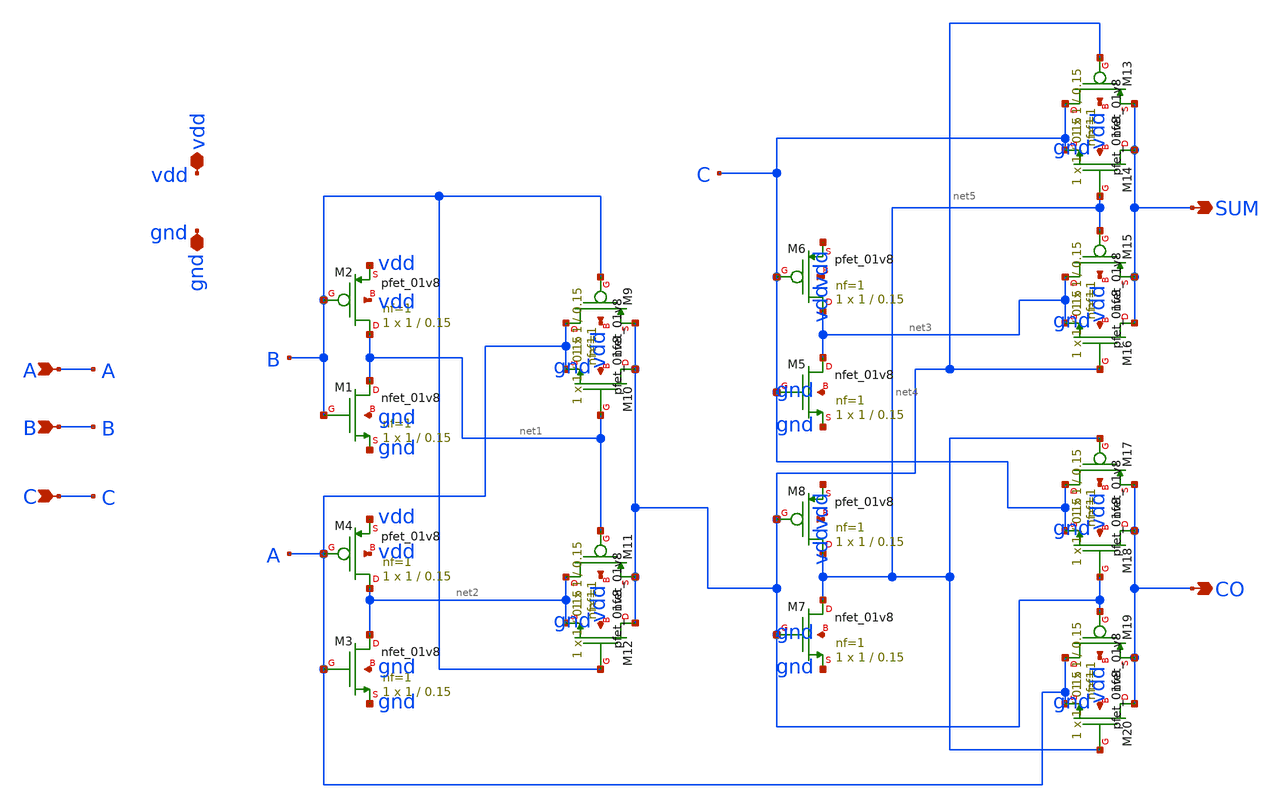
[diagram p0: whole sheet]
** sch_path: FA20T.sch
**.subckt FA20T A B C SUM CO vdd gnd
*.ipin A
*.ipin B
*.ipin C
*.opin SUM
*.opin CO
*.iopin vdd
*.iopin gnd
XM1 net1 B gnd gnd sky130_fd_pr__nfet_01v8 L=0.15 W=1 nf=1 ad='int((1 + 1)/2) * 1 / 1 * 0.29' as='int((1 + 2)/2) * 1 / 1 * 0.29'
+ pd='2*int((1 + 1)/2) * (1 / 1 + 0.29)' ps='2*int((1 + 2)/2) * (1 / 1 + 0.29)' nrd='0.29 / 1 ' nrs='0.29 / 1 '
+ sa=0 sb=0 sd=0 mult=1 m=1
XM2 net1 B vdd vdd sky130_fd_pr__pfet_01v8 L=0.15 W=1 nf=1 ad='int((1 + 1)/2) * 1 / 1 * 0.29' as='int((1 + 2)/2) * 1 / 1 * 0.29'
+ pd='2*int((1 + 1)/2) * (1 / 1 + 0.29)' ps='2*int((1 + 2)/2) * (1 / 1 + 0.29)' nrd='0.29 / 1 ' nrs='0.29 / 1 '
+ sa=0 sb=0 sd=0 mult=1 m=1
XM3 net2 A gnd gnd sky130_fd_pr__nfet_01v8 L=0.15 W=1 nf=1 ad='int((1 + 1)/2) * 1 / 1 * 0.29' as='int((1 + 2)/2) * 1 / 1 * 0.29'
+ pd='2*int((1 + 1)/2) * (1 / 1 + 0.29)' ps='2*int((1 + 2)/2) * (1 / 1 + 0.29)' nrd='0.29 / 1 ' nrs='0.29 / 1 '
+ sa=0 sb=0 sd=0 mult=1 m=1
XM4 net2 A vdd vdd sky130_fd_pr__pfet_01v8 L=0.15 W=1 nf=1 ad='int((1 + 1)/2) * 1 / 1 * 0.29' as='int((1 + 2)/2) * 1 / 1 * 0.29'
+ pd='2*int((1 + 1)/2) * (1 / 1 + 0.29)' ps='2*int((1 + 2)/2) * (1 / 1 + 0.29)' nrd='0.29 / 1 ' nrs='0.29 / 1 '
+ sa=0 sb=0 sd=0 mult=1 m=1
XM5 net3 C gnd gnd sky130_fd_pr__nfet_01v8 L=0.15 W=1 nf=1 ad='int((1 + 1)/2) * 1 / 1 * 0.29' as='int((1 + 2)/2) * 1 / 1 * 0.29'
+ pd='2*int((1 + 1)/2) * (1 / 1 + 0.29)' ps='2*int((1 + 2)/2) * (1 / 1 + 0.29)' nrd='0.29 / 1 ' nrs='0.29 / 1 '
+ sa=0 sb=0 sd=0 mult=1 m=1
XM6 net3 C vdd vdd sky130_fd_pr__pfet_01v8 L=0.15 W=1 nf=1 ad='int((1 + 1)/2) * 1 / 1 * 0.29' as='int((1 + 2)/2) * 1 / 1 * 0.29'
+ pd='2*int((1 + 1)/2) * (1 / 1 + 0.29)' ps='2*int((1 + 2)/2) * (1 / 1 + 0.29)' nrd='0.29 / 1 ' nrs='0.29 / 1 '
+ sa=0 sb=0 sd=0 mult=1 m=1
XM7 net4 net5 gnd gnd sky130_fd_pr__nfet_01v8 L=0.15 W=1 nf=1 ad='int((1 + 1)/2) * 1 / 1 * 0.29' as='int((1 + 2)/2) * 1 / 1 * 0.29'
+ pd='2*int((1 + 1)/2) * (1 / 1 + 0.29)' ps='2*int((1 + 2)/2) * (1 / 1 + 0.29)' nrd='0.29 / 1 ' nrs='0.29 / 1 '
+ sa=0 sb=0 sd=0 mult=1 m=1
XM8 net4 net5 vdd vdd sky130_fd_pr__pfet_01v8 L=0.15 W=1 nf=1 ad='int((1 + 1)/2) * 1 / 1 * 0.29' as='int((1 + 2)/2) * 1 / 1 * 0.29'
+ pd='2*int((1 + 1)/2) * (1 / 1 + 0.29)' ps='2*int((1 + 2)/2) * (1 / 1 + 0.29)' nrd='0.29 / 1 ' nrs='0.29 / 1 '
+ sa=0 sb=0 sd=0 mult=1 m=1
XM9 A B net5 vdd sky130_fd_pr__pfet_01v8 L=0.15 W=1 nf=1 ad='int((1 + 1)/2) * 1 / 1 * 0.29' as='int((1 + 2)/2) * 1 / 1 * 0.29'
+ pd='2*int((1 + 1)/2) * (1 / 1 + 0.29)' ps='2*int((1 + 2)/2) * (1 / 1 + 0.29)' nrd='0.29 / 1 ' nrs='0.29 / 1 '
+ sa=0 sb=0 sd=0 mult=1 m=1
XM10 net5 net1 A gnd sky130_fd_pr__nfet_01v8 L=0.15 W=1 nf=1 ad='int((1 + 1)/2) * 1 / 1 * 0.29' as='int((1 + 2)/2) * 1 / 1 * 0.29'
+ pd='2*int((1 + 1)/2) * (1 / 1 + 0.29)' ps='2*int((1 + 2)/2) * (1 / 1 + 0.29)' nrd='0.29 / 1 ' nrs='0.29 / 1 '
+ sa=0 sb=0 sd=0 mult=1 m=1
XM11 net2 net1 net5 vdd sky130_fd_pr__pfet_01v8 L=0.15 W=1 nf=1 ad='int((1 + 1)/2) * 1 / 1 * 0.29' as='int((1 + 2)/2) * 1 / 1 * 0.29'
+ pd='2*int((1 + 1)/2) * (1 / 1 + 0.29)' ps='2*int((1 + 2)/2) * (1 / 1 + 0.29)' nrd='0.29 / 1 ' nrs='0.29 / 1 '
+ sa=0 sb=0 sd=0 mult=1 m=1
XM12 net5 B net2 gnd sky130_fd_pr__nfet_01v8 L=0.15 W=1 nf=1 ad='int((1 + 1)/2) * 1 / 1 * 0.29' as='int((1 + 2)/2) * 1 / 1 * 0.29'
+ pd='2*int((1 + 1)/2) * (1 / 1 + 0.29)' ps='2*int((1 + 2)/2) * (1 / 1 + 0.29)' nrd='0.29 / 1 ' nrs='0.29 / 1 '
+ sa=0 sb=0 sd=0 mult=1 m=1
XM13 C net5 SUM vdd sky130_fd_pr__pfet_01v8 L=0.15 W=1 nf=1 ad='int((1 + 1)/2) * 1 / 1 * 0.29' as='int((1 + 2)/2) * 1 / 1 * 0.29'
+ pd='2*int((1 + 1)/2) * (1 / 1 + 0.29)' ps='2*int((1 + 2)/2) * (1 / 1 + 0.29)' nrd='0.29 / 1 ' nrs='0.29 / 1 '
+ sa=0 sb=0 sd=0 mult=1 m=1
XM14 SUM net4 C gnd sky130_fd_pr__nfet_01v8 L=0.15 W=1 nf=1 ad='int((1 + 1)/2) * 1 / 1 * 0.29' as='int((1 + 2)/2) * 1 / 1 * 0.29'
+ pd='2*int((1 + 1)/2) * (1 / 1 + 0.29)' ps='2*int((1 + 2)/2) * (1 / 1 + 0.29)' nrd='0.29 / 1 ' nrs='0.29 / 1 '
+ sa=0 sb=0 sd=0 mult=1 m=1
XM15 net3 net4 SUM vdd sky130_fd_pr__pfet_01v8 L=0.15 W=1 nf=1 ad='int((1 + 1)/2) * 1 / 1 * 0.29' as='int((1 + 2)/2) * 1 / 1 * 0.29'
+ pd='2*int((1 + 1)/2) * (1 / 1 + 0.29)' ps='2*int((1 + 2)/2) * (1 / 1 + 0.29)' nrd='0.29 / 1 ' nrs='0.29 / 1 '
+ sa=0 sb=0 sd=0 mult=1 m=1
XM16 SUM net5 net3 gnd sky130_fd_pr__nfet_01v8 L=0.15 W=1 nf=1 ad='int((1 + 1)/2) * 1 / 1 * 0.29' as='int((1 + 2)/2) * 1 / 1 * 0.29'
+ pd='2*int((1 + 1)/2) * (1 / 1 + 0.29)' ps='2*int((1 + 2)/2) * (1 / 1 + 0.29)' nrd='0.29 / 1 ' nrs='0.29 / 1 '
+ sa=0 sb=0 sd=0 mult=1 m=1
XM17 C net4 CO vdd sky130_fd_pr__pfet_01v8 L=0.15 W=1 nf=1 ad='int((1 + 1)/2) * 1 / 1 * 0.29' as='int((1 + 2)/2) * 1 / 1 * 0.29'
+ pd='2*int((1 + 1)/2) * (1 / 1 + 0.29)' ps='2*int((1 + 2)/2) * (1 / 1 + 0.29)' nrd='0.29 / 1 ' nrs='0.29 / 1 '
+ sa=0 sb=0 sd=0 mult=1 m=1
XM18 CO net5 C gnd sky130_fd_pr__nfet_01v8 L=0.15 W=1 nf=1 ad='int((1 + 1)/2) * 1 / 1 * 0.29' as='int((1 + 2)/2) * 1 / 1 * 0.29'
+ pd='2*int((1 + 1)/2) * (1 / 1 + 0.29)' ps='2*int((1 + 2)/2) * (1 / 1 + 0.29)' nrd='0.29 / 1 ' nrs='0.29 / 1 '
+ sa=0 sb=0 sd=0 mult=1 m=1
XM19 A net5 CO vdd sky130_fd_pr__pfet_01v8 L=0.15 W=1 nf=1 ad='int((1 + 1)/2) * 1 / 1 * 0.29' as='int((1 + 2)/2) * 1 / 1 * 0.29'
+ pd='2*int((1 + 1)/2) * (1 / 1 + 0.29)' ps='2*int((1 + 2)/2) * (1 / 1 + 0.29)' nrd='0.29 / 1 ' nrs='0.29 / 1 '
+ sa=0 sb=0 sd=0 mult=1 m=1
XM20 CO net4 A gnd sky130_fd_pr__nfet_01v8 L=0.15 W=1 nf=1 ad='int((1 + 1)/2) * 1 / 1 * 0.29' as='int((1 + 2)/2) * 1 / 1 * 0.29'
+ pd='2*int((1 + 1)/2) * (1 / 1 + 0.29)' ps='2*int((1 + 2)/2) * (1 / 1 + 0.29)' nrd='0.29 / 1 ' nrs='0.29 / 1 '
+ sa=0 sb=0 sd=0 mult=1 m=1
**.ends
.end
